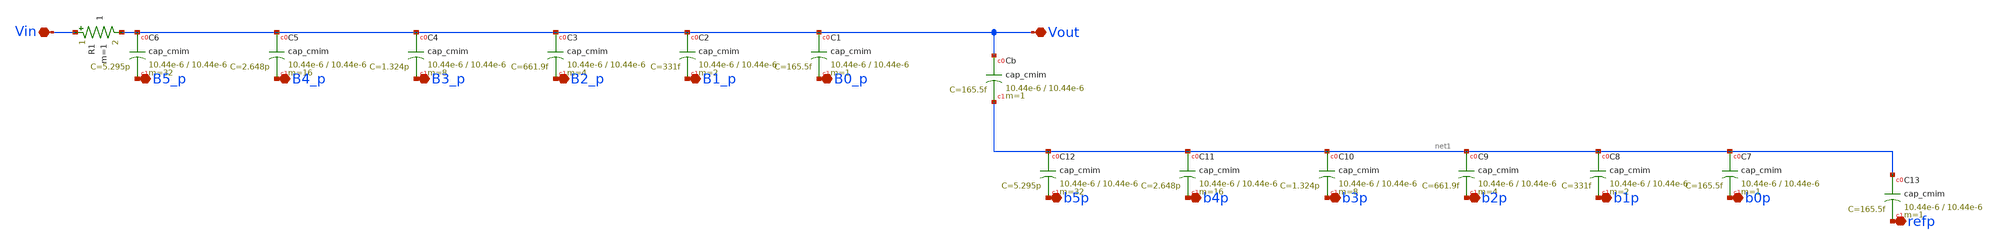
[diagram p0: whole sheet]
** sch_path: schematic/cdac_12bit_split_single.sch
**.subckt cdac_12bit_split_single B0_p B1_p B2_p B3_p B4_p B5_p Vout b0p b1p b2p b3p b4p b5p refp
*+ Vin
*.iopin B0_p
*.iopin B1_p
*.iopin B2_p
*.iopin B3_p
*.iopin B4_p
*.iopin B5_p
*.iopin Vout
*.iopin b0p
*.iopin b1p
*.iopin b2p
*.iopin b3p
*.iopin b4p
*.iopin b5p
*.iopin refp
*.iopin Vin
XC1 Vout B0_p cap_cmim w=10.44e-6 l=10.44e-6 m=1 mm_ok=1
XC2 Vout B1_p cap_cmim w=10.44e-6 l=10.44e-6 m=2 mm_ok=1
XC3 Vout B2_p cap_cmim w=10.44e-6 l=10.44e-6 m=4 mm_ok=1
XC4 Vout B3_p cap_cmim w=10.44e-6 l=10.44e-6 m=8 mm_ok=1
XC5 Vout B4_p cap_cmim w=10.44e-6 l=10.44e-6 m=16 mm_ok=1
XC6 Vout B5_p cap_cmim w=10.44e-6 l=10.44e-6 m=32 mm_ok=1
XCb Vout net1 cap_cmim w=10.44e-6 l=10.44e-6 m=1 mm_ok=1
XC7 net1 b0p cap_cmim w=10.44e-6 l=10.44e-6 m=1 mm_ok=1
XC8 net1 b1p cap_cmim w=10.44e-6 l=10.44e-6 m=2 mm_ok=1
XC9 net1 b2p cap_cmim w=10.44e-6 l=10.44e-6 m=4 mm_ok=1
XC10 net1 b3p cap_cmim w=10.44e-6 l=10.44e-6 m=8 mm_ok=1
XC11 net1 b4p cap_cmim w=10.44e-6 l=10.44e-6 m=16 mm_ok=1
XC12 net1 b5p cap_cmim w=10.44e-6 l=10.44e-6 m=32 mm_ok=1
XC13 net1 refp cap_cmim w=10.44e-6 l=10.44e-6 m=1 mm_ok=1
R1 Vin Vout 1 m=1
**.ends
.end
